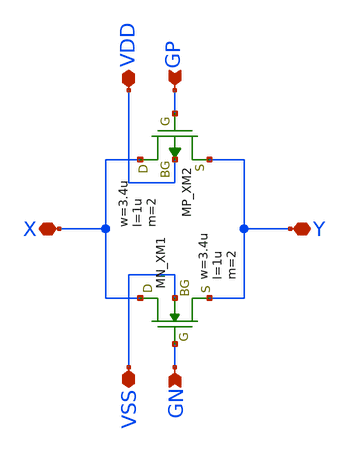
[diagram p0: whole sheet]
** sch_path: member_project/imager/YuMaehashi/design/aswx2.sch
**.subckt aswx2 Y GP GN X VDD VSS
*.iopin Y
*.ipin GP
*.ipin GN
*.iopin X
*.iopin VDD
*.iopin VSS
XXM1 X GN Y VSS NMOS w=3.4u l=1u nrd=0 nrs=0 m=2
XXM2 X GP Y VDD PMOS w=3.4u l=1u nrd=0 nrs=0 m=2
**.ends
.end
